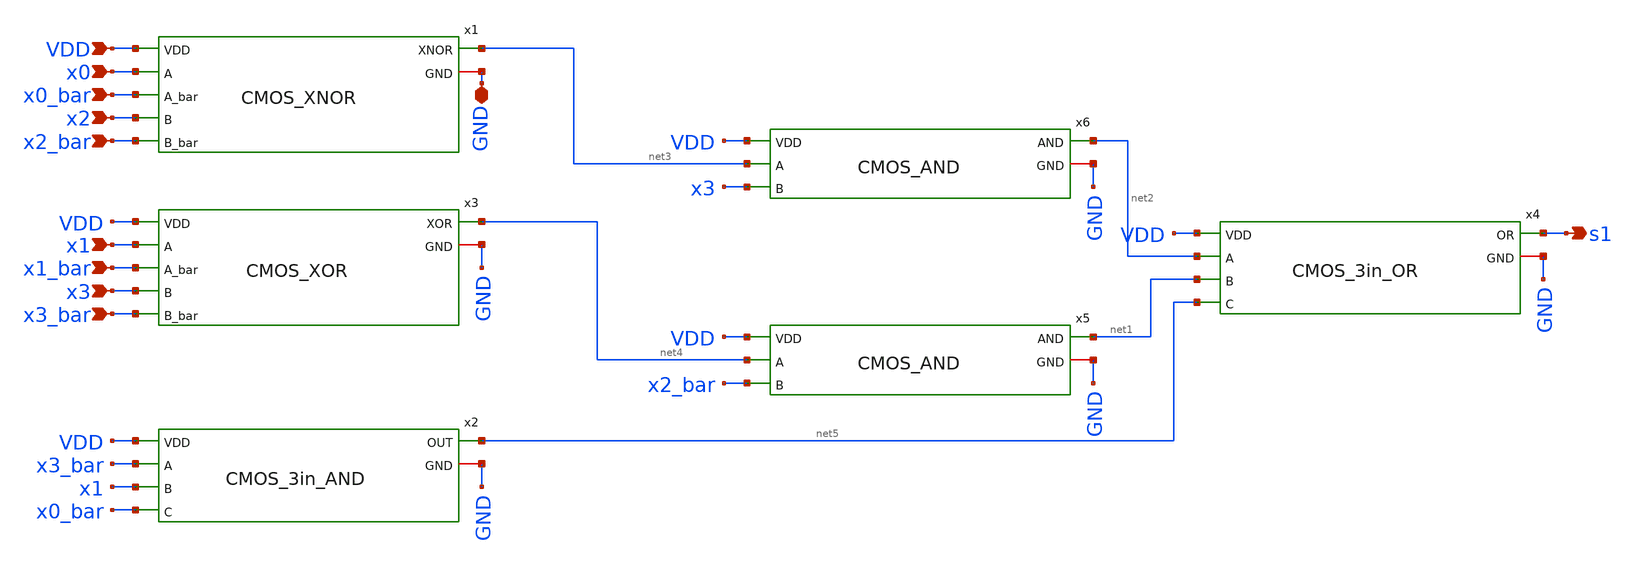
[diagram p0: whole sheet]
** sch_path: skywater_stuff/CMOS_s1_flat.sch
**.subckt CMOS_s1_flat GND x0 x0_bar x1 x1_bar x2 x2_bar x3 x3_bar s1 VDD
*.iopin GND
*.ipin x0
*.ipin x0_bar
*.ipin x1
*.ipin x1_bar
*.ipin x2
*.ipin x2_bar
*.ipin x3
*.ipin x3_bar
*.opin s1
*.ipin VDD
x1 x0 x0_bar x2 x2_bar net3 GND VDD CMOS_XNOR
x4 net2 net1 net5 s1 GND VDD CMOS_3in_OR
x3 x1 x1_bar x3 x3_bar net4 GND VDD CMOS_XOR
x6 net3 x3 net2 GND VDD CMOS_AND
x5 net4 x2_bar net1 GND VDD CMOS_AND
x2 x3_bar x1 x0_bar net5 GND VDD CMOS_3in_AND
**.ends
.end
